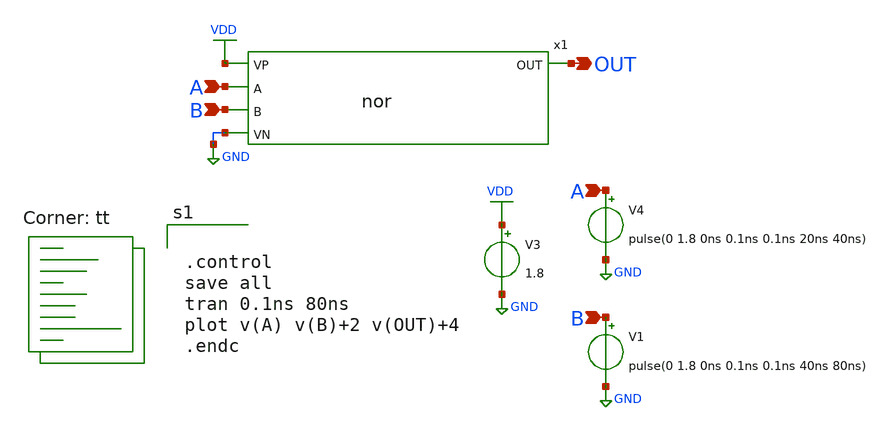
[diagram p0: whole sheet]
** sch_path: basic_cell/single_cell/nor/tb_xschem_nor.sch
**.subckt tb_xschem_nor A B A B OUT
*.ipin A
*.ipin B
*.ipin A
*.ipin B
*.opin OUT
x1 VDD A B OUT GND nor
V3 VDD GND 1.8
V4 A GND pulse(0 1.8 0ns 0.1ns 0.1ns 20ns 40ns)
V1 B GND pulse(0 1.8 0ns 0.1ns 0.1ns 40ns 80ns)
**** begin user architecture code
.lib $::SKYWATER_MODELS/sky130.lib.spice tt


.control
save all
tran 0.1ns 80ns
plot v(A) v(B)+2 v(OUT)+4
.endc


**** end user architecture code
**.ends

* expanding   symbol:  nor.sym # of pins=5
** sym_path: basic_cell/single_cell/nor/nor.sym
** sch_path: basic_cell/single_cell/nor/nor.sch
.subckt nor VP A B OUT VN
*.ipin A
*.ipin B
*.ipin VP
*.ipin VN
*.opin OUT
XM1 OUT A VN VN sky130_fd_pr__nfet_01v8 L=0.15 W=1 nf=1 ad='int((nf+1)/2) * W/nf * 0.29' as='int((nf+2)/2) * W/nf * 0.29'
+ pd='2*int((nf+1)/2) * (W/nf + 0.29)' ps='2*int((nf+2)/2) * (W/nf + 0.29)' nrd='0.29 / W' nrs='0.29 / W'
+ sa=0 sb=0 sd=0 mult=1 m=1
XM2 OUT B VN VN sky130_fd_pr__nfet_01v8 L=0.15 W=1 nf=1 ad='int((nf+1)/2) * W/nf * 0.29' as='int((nf+2)/2) * W/nf * 0.29'
+ pd='2*int((nf+1)/2) * (W/nf + 0.29)' ps='2*int((nf+2)/2) * (W/nf + 0.29)' nrd='0.29 / W' nrs='0.29 / W'
+ sa=0 sb=0 sd=0 mult=1 m=1
XM3 OUT B net1 VP sky130_fd_pr__pfet_01v8 L=0.15 W=3 nf=1 ad='int((nf+1)/2) * W/nf * 0.29' as='int((nf+2)/2) * W/nf * 0.29'
+ pd='2*int((nf+1)/2) * (W/nf + 0.29)' ps='2*int((nf+2)/2) * (W/nf + 0.29)' nrd='0.29 / W' nrs='0.29 / W'
+ sa=0 sb=0 sd=0 mult=1 m=1
XM4 net1 A VP VP sky130_fd_pr__pfet_01v8 L=0.15 W=3 nf=1 ad='int((nf+1)/2) * W/nf * 0.29' as='int((nf+2)/2) * W/nf * 0.29'
+ pd='2*int((nf+1)/2) * (W/nf + 0.29)' ps='2*int((nf+2)/2) * (W/nf + 0.29)' nrd='0.29 / W' nrs='0.29 / W'
+ sa=0 sb=0 sd=0 mult=1 m=1
.ends

.GLOBAL VDD
.GLOBAL GND
.end
